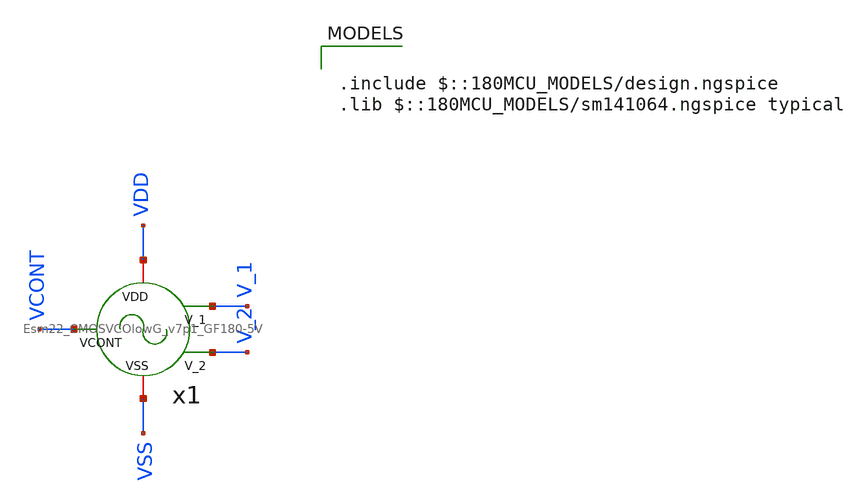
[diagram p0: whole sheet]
** sch_path: xschem/vco/tb_CMOSVCO_v7p1_GF180-5V.sch
**.subckt tb_CMOSVCO_v7p1_GF180-5V
x1 VCONT VSS VDD V_1 V_2 Esm22_CMOSVCOlowG_v7p1_GF180-5V
**** begin user architecture code

vvdd vdd 0 dc 5
vvss vss 0 0
vvcont VCONT 0 dc 1.65
*.option temp = 200
.ic v(V_1) = 0
.ic v(V_2) = 5
.save v(V_1)

.control
*   compose vin_var start=0.1 stop=0.91 step=0.06
   compose vin_var start=1.1 stop=3.31 step=0.12
   foreach val $&vin_var
     alter vvcont $val
     tran 5n 50u
   end
wrdata
+ /foss/designs/SSCS-Chipathon-2025_AC3E-Chile-team/xschem/vco/simulations/data_CMOSVCOlowG_v7p1_GF180-5V.txt v(V_1) tran1.v(V_1) tran2.v(V_1) tran3.v(V_1) tran4.v(V_1) tran5.v(V_1) tran6.v(V_1) tran7.v(V_1)
+ tran8.v(V_1) tran9.v(V_1) tran10.v(V_1) tran11.v(V_1) tran12.v(V_1) tran13.v(V_1) tran14.v(V_1) tran15.v(V_1)
+ tran16.v(V_1) tran17.v(V_1) tran18.v(V_1) tran19.v(V_1)
*wrdata /foss/designs/Chipathon2025_Esm22/data_CMOSVCOlowG_v4p2_IHP.txt v(V_1) tran1.v(V_1)
*+ tran2.v(V_1) tran3.v(V_1) tran4.v(V_1) tran5.v(V_1) tran6.v(V_1) tran7.v(V_1) tran8.v(V_1) tran9.v(V_1)
*+ tran10.v(V_1) tran11.v(V_1) tran12.v(V_1) tran13.v(V_1) tran14.v(V_1)
plot tran1.v(V_1) (tran10.v(V_1)+4) (tran19.v(V_1)+8)
*plot tran1.v(V_1) (tran7.v(V_1)+4) (tran14.v(V_1)+8)
.endc



.include $::180MCU_MODELS/design.ngspice
.lib $::180MCU_MODELS/sm141064.ngspice typical

**** end user architecture code
**.ends

* expanding   symbol:  vco/Esm22_CMOSVCOlowG_v7p1_GF180-5V.sym # of pins=5
** sym_path: xschem/vco/Esm22_CMOSVCOlowG_v7p1_GF180-5V.sym
** sch_path: xschem/vco/Esm22_CMOSVCOlowG_v7p1_GF180-5V.sch
.subckt Esm22_CMOSVCOlowG_v7p1_GF180-5V VCONT VSS VDD V_1 V_2
*.ipin VCONT
*.iopin VDD
*.iopin VSS
*.opin V_1
*.opin V_2
x1 VDD VCONT V_1 V_5 VSS stage_v7p1_GF180-5V
x2 VDD VCONT V_2 V_1 VSS stage_v7p1_GF180-5V
x3 VDD VCONT V_3 V_2 VSS stage_v7p1_GF180-5V
x4 VDD VCONT V_4 V_3 VSS stage_v7p1_GF180-5V
x5 VDD VCONT V_5 V_4 VSS stage_v7p1_GF180-5V
.ends


* expanding   symbol:  vco/stage_v7p1_GF180-5V.sym # of pins=5
** sym_path: xschem/vco/stage_v7p1_GF180-5V.sym
** sch_path: xschem/vco/stage_v7p1_GF180-5V.sch
.subckt stage_v7p1_GF180-5V VDD VCONT VOUT VIN VSS
*.ipin VIN
*.opin VOUT
*.iopin VDD
*.iopin VSS
*.ipin VCONT
XMN1 net4 net4 VSS VSS nfet_05v0 L=0.70u W=7u nf=7 ad='int((nf+1)/2) * W/nf * 0.18u' as='int((nf+2)/2) * W/nf * 0.18u'
+ pd='2*int((nf+1)/2) * (W/nf + 0.18u)' ps='2*int((nf+2)/2) * (W/nf + 0.18u)' nrd='0.18u / W' nrs='0.18u / W'
+ sa=0 sb=0 sd=0 m=1
XMN2 net3 net4 VSS VSS nfet_05v0 L=0.70u W=7u nf=7 ad='int((nf+1)/2) * W/nf * 0.18u' as='int((nf+2)/2) * W/nf * 0.18u'
+ pd='2*int((nf+1)/2) * (W/nf + 0.18u)' ps='2*int((nf+2)/2) * (W/nf + 0.18u)' nrd='0.18u / W' nrs='0.18u / W'
+ sa=0 sb=0 sd=0 m=1
XMN3 net2 net4 VSS VSS nfet_05v0 L=0.70u W=4u nf=4 ad='int((nf+1)/2) * W/nf * 0.18u' as='int((nf+2)/2) * W/nf * 0.18u'
+ pd='2*int((nf+1)/2) * (W/nf + 0.18u)' ps='2*int((nf+2)/2) * (W/nf + 0.18u)' nrd='0.18u / W' nrs='0.18u / W'
+ sa=0 sb=0 sd=0 m=1
XMN4 VOUT VIN net2 VSS nfet_05v0 L=5u W=2u nf=1 ad='int((nf+1)/2) * W/nf * 0.18u' as='int((nf+2)/2) * W/nf * 0.18u'
+ pd='2*int((nf+1)/2) * (W/nf + 0.18u)' ps='2*int((nf+2)/2) * (W/nf + 0.18u)' nrd='0.18u / W' nrs='0.18u / W'
+ sa=0 sb=0 sd=0 m=1
XMP2 net3 net3 VDD VDD pfet_05v0 L=4u W=8u nf=8 ad='int((nf+1)/2) * W/nf * 0.18u' as='int((nf+2)/2) * W/nf * 0.18u'
+ pd='2*int((nf+1)/2) * (W/nf + 0.18u)' ps='2*int((nf+2)/2) * (W/nf + 0.18u)' nrd='0.18u / W' nrs='0.18u / W'
+ sa=0 sb=0 sd=0 m=1
XMP3 net1 net3 VDD VDD pfet_05v0 L=4u W=5u nf=5 ad='int((nf+1)/2) * W/nf * 0.18u' as='int((nf+2)/2) * W/nf * 0.18u'
+ pd='2*int((nf+1)/2) * (W/nf + 0.18u)' ps='2*int((nf+2)/2) * (W/nf + 0.18u)' nrd='0.18u / W' nrs='0.18u / W'
+ sa=0 sb=0 sd=0 m=1
XMP1 net4 VCONT VDD VDD pfet_05v0 L=7u W=0.5u nf=1 ad='int((nf+1)/2) * W/nf * 0.18u' as='int((nf+2)/2) * W/nf * 0.18u'
+ pd='2*int((nf+1)/2) * (W/nf + 0.18u)' ps='2*int((nf+2)/2) * (W/nf + 0.18u)' nrd='0.18u / W' nrs='0.18u / W'
+ sa=0 sb=0 sd=0 m=1
XMP4 VOUT VIN net1 VDD pfet_05v0 L=5u W=5u nf=1 ad='int((nf+1)/2) * W/nf * 0.18u' as='int((nf+2)/2) * W/nf * 0.18u'
+ pd='2*int((nf+1)/2) * (W/nf + 0.18u)' ps='2*int((nf+2)/2) * (W/nf + 0.18u)' nrd='0.18u / W' nrs='0.18u / W'
+ sa=0 sb=0 sd=0 m=1
XMP5 net4 VSS VDD VDD pfet_05v0 L=7u W=0.5u nf=1 ad='int((nf+1)/2) * W/nf * 0.18u' as='int((nf+2)/2) * W/nf * 0.18u'
+ pd='2*int((nf+1)/2) * (W/nf + 0.18u)' ps='2*int((nf+2)/2) * (W/nf + 0.18u)' nrd='0.18u / W' nrs='0.18u / W'
+ sa=0 sb=0 sd=0 m=1
.ends

.end
